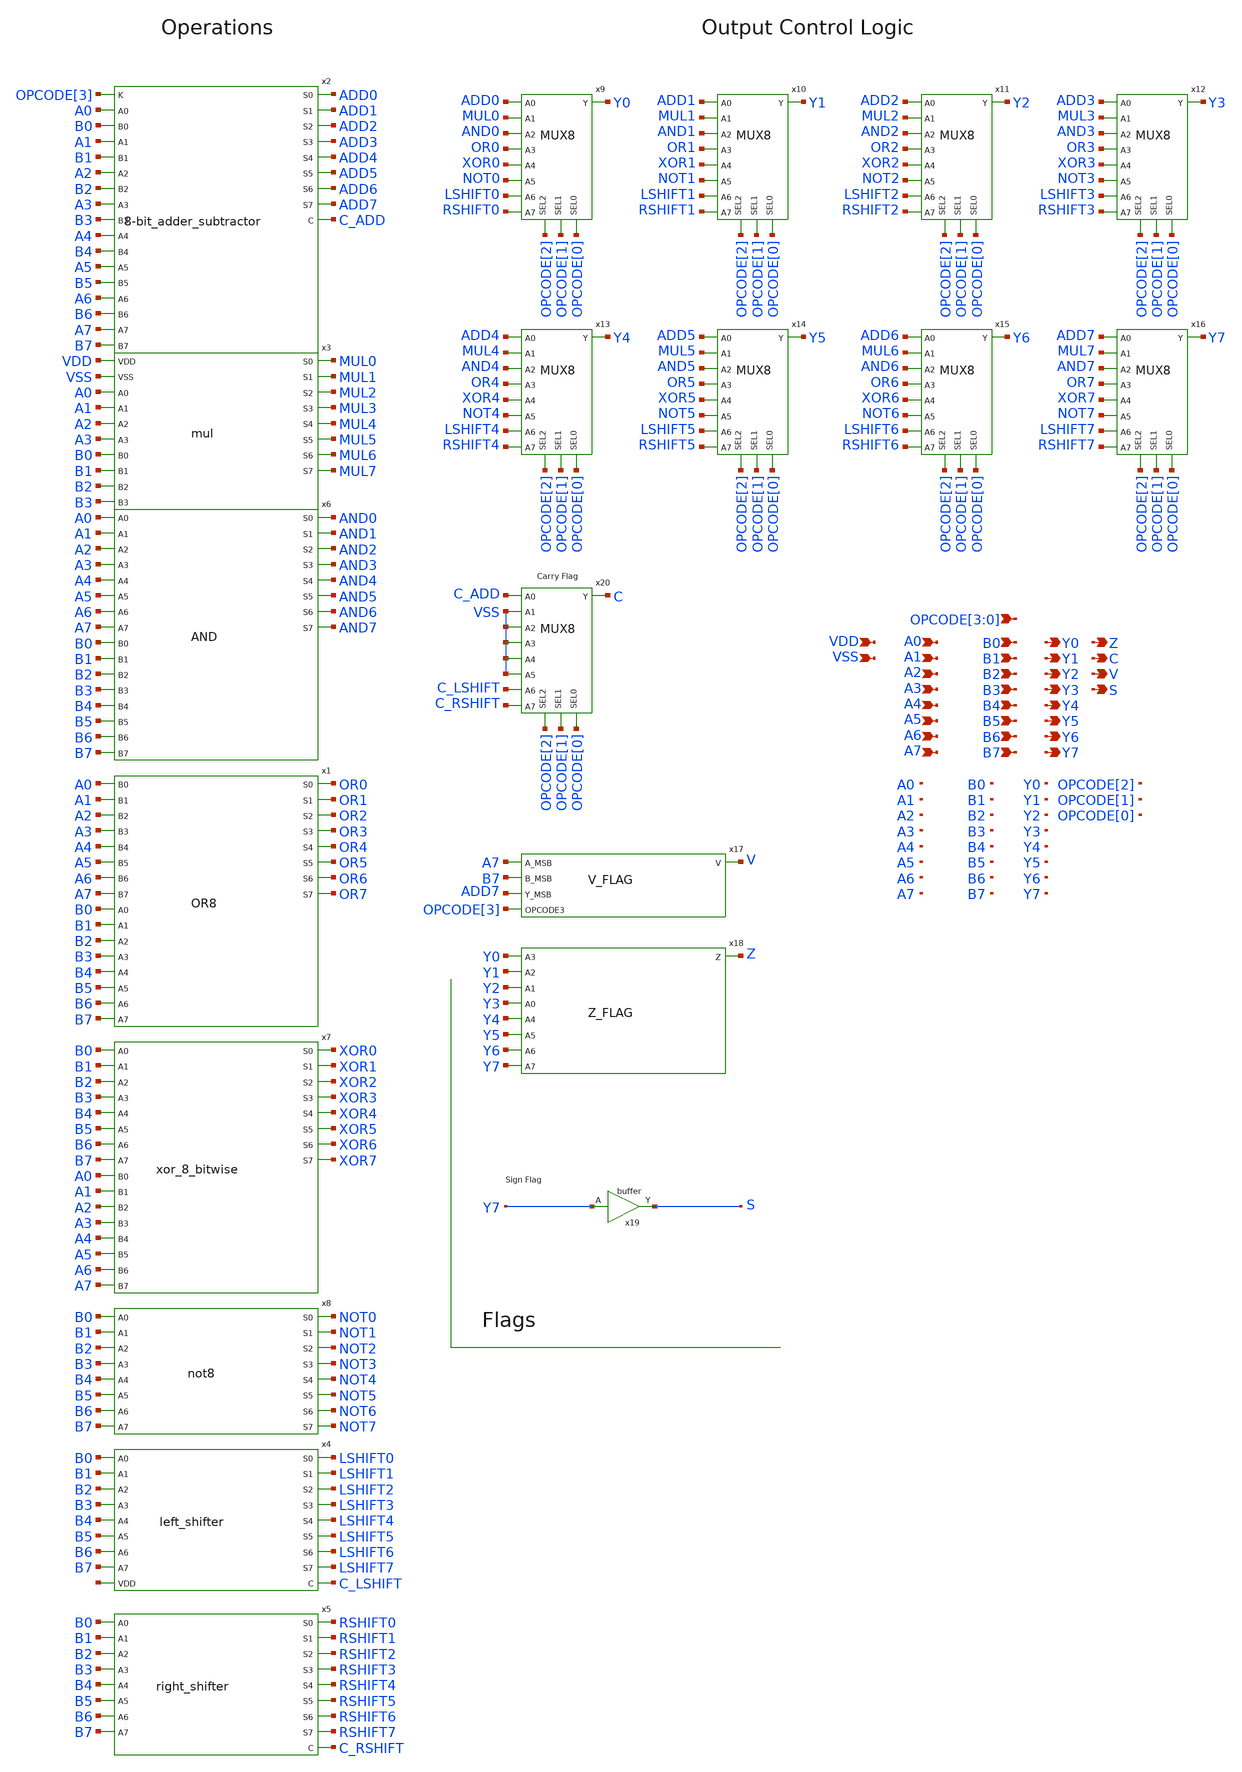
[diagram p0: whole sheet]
** sch_path: design/xschem/ALU/alu.sch
**.subckt alu A7 A6 A5 A4 A3 A2 A1 A0 B1 B2 B3 B0 B6 B7 B5 Y0 Y1 Y2 Y3 Y4 Y5 Y6 Y7
*+ OPCODE[3],OPCODE[2],OPCODE[1],OPCODE[0] Z C V S B4 VSS VDD
*.ipin A7
*.ipin A6
*.ipin A5
*.ipin A4
*.ipin A3
*.ipin A2
*.ipin A1
*.ipin A0
*.ipin B1
*.ipin B2
*.ipin B3
*.ipin B0
*.ipin B6
*.ipin B7
*.ipin B5
*.opin Y0
*.opin Y1
*.opin Y2
*.opin Y3
*.opin Y4
*.opin Y5
*.opin Y6
*.opin Y7
*.ipin OPCODE[3],OPCODE[2],OPCODE[1],OPCODE[0]
*.opin Z
*.opin C
*.opin V
*.opin S
*.ipin B4
*.ipin VSS
*.ipin VDD
x4 B0 B1 B2 B3 B4 B5 B6 B7 net1 LSHIFT0 LSHIFT1 LSHIFT2 LSHIFT3 LSHIFT4 LSHIFT5 LSHIFT6 LSHIFT7
+ C_LSHIFT left_shifter
x5 B0 B1 B2 B3 B4 B5 B6 B7 RSHIFT0 RSHIFT1 RSHIFT2 RSHIFT3 RSHIFT4 RSHIFT5 RSHIFT6 RSHIFT7 C_RSHIFT
+ VSS VDD right_shifter
x6 AND0 A0 AND1 A1 A2 AND2 A3 AND3 A4 AND4 A5 AND5 AND6 A6 A7 AND7 B0 B1 B2 B3 B4 B5 B6 B7 VSS VDD
+ AND
x8 B0 B1 B2 B3 B4 B5 B6 B7 NOT0 NOT1 NOT2 NOT3 NOT4 NOT5 NOT6 NOT7 not8
x1 A0 OR0 OR1 A1 A2 OR2 A3 OR3 A4 OR4 A5 OR5 A6 OR6 A7 OR7 B0 B1 B2 B3 B4 B5 B6 B7 OR8
x7 B0 XOR0 A0 B1 XOR1 A1 B2 XOR2 A2 XOR3 B3 A3 XOR4 B4 A4 XOR5 B5 A5 B6 XOR6 A6 XOR7 B7 A7
+ xor_8_bitwise
x9 OPCODE[0] OPCODE[1] OPCODE[2] ADD0 MUL0 AND0 OR0 XOR0 NOT0 Y0 LSHIFT0 RSHIFT0 MUX8
x10 OPCODE[0] OPCODE[1] OPCODE[2] ADD1 MUL1 AND1 OR1 XOR1 NOT1 Y1 LSHIFT1 RSHIFT1 MUX8
x11 OPCODE[0] OPCODE[1] OPCODE[2] ADD2 MUL2 AND2 OR2 XOR2 NOT2 Y2 LSHIFT2 RSHIFT2 MUX8
x12 OPCODE[0] OPCODE[1] OPCODE[2] ADD3 MUL3 AND3 OR3 XOR3 NOT3 Y3 LSHIFT3 RSHIFT3 MUX8
x13 OPCODE[0] OPCODE[1] OPCODE[2] ADD4 MUL4 AND4 OR4 XOR4 NOT4 Y4 LSHIFT4 RSHIFT4 MUX8
x14 OPCODE[0] OPCODE[1] OPCODE[2] ADD5 MUL5 AND5 OR5 XOR5 NOT5 Y5 LSHIFT5 RSHIFT5 MUX8
x15 OPCODE[0] OPCODE[1] OPCODE[2] ADD6 MUL6 AND6 OR6 XOR6 NOT6 Y6 LSHIFT6 RSHIFT6 MUX8
x16 OPCODE[0] OPCODE[1] OPCODE[2] ADD7 MUL7 AND7 OR7 XOR7 NOT7 Y7 LSHIFT7 RSHIFT7 MUX8
x3 VDD VSS A0 A1 A2 A3 B0 B1 B2 B3 MUL0 MUL1 MUL2 MUL5 MUL4 MUL3 MUL7 MUL6 VSS VDD mul
x18 Y0 Y1 Y2 Y3 Z Y4 Y5 Y6 Y7 Z_FLAG
x19 Y7 VSS VDD S buffer
x20 OPCODE[0] OPCODE[1] OPCODE[2] C_ADD VSS VSS VSS VSS VSS C C_LSHIFT C_RSHIFT MUX8
x2 OPCODE[3] ADD0 A0 B0 ADD1 A1 B1 A2 ADD2 B2 A3 ADD3 B3 A4 ADD4 B4 A5 ADD5 B5 ADD6 A6 B6 ADD7 A7
+ C_ADD B7 VSS VDD 8-bit_adder_subtractor
x17 A7 B7 ADD7 V OPCODE[3] VSS VDD V_FLAG
**.ends
.end
